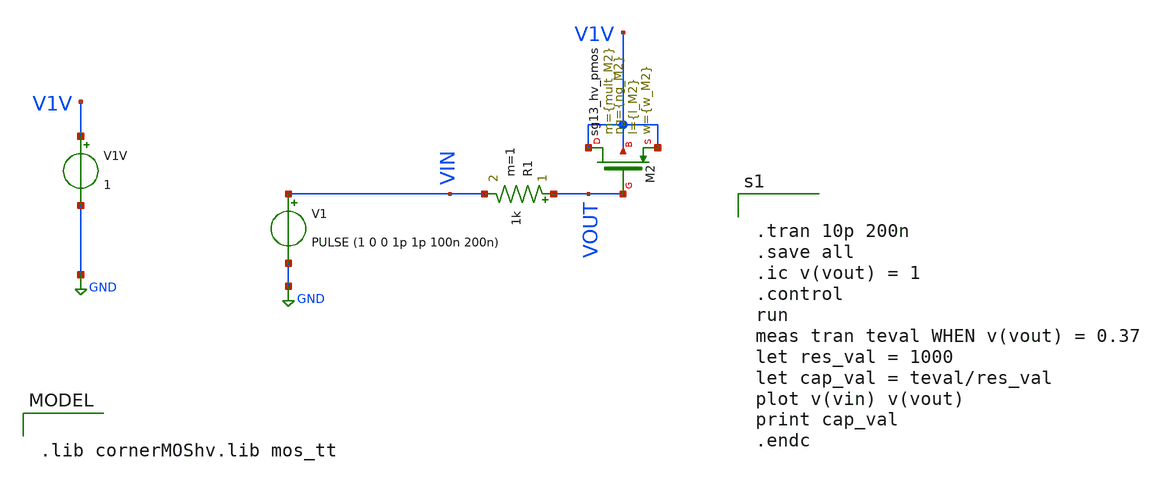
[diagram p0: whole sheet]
** sch_path: xschem/TB_hvPMOS_cgate-ext.sch
**.subckt TB_hvPMOS_cgate-ext
R1 VOUT VIN 1k m=1
V1 VIN GND PULSE (1 0 0 1p 1p 100n 200n)
XM2 V1V VOUT V1V V1V sg13_hv_pmos w={w_M2} l={l_M2} ng={ng_M2} m={mult_M2} mm_ok=1
V1V V1V GND 1
**** begin user architecture code


.tran 10p 200n
.save all
.ic v(vout) = 1
.control
run
meas tran teval WHEN v(vout) = 0.37
let res_val = 1000
let cap_val = teval/res_val
plot v(vin) v(vout)
print cap_val
.endc




.param temp=27

.param mult_M2 = 1200
.param w_M2 =10u
*.param l_M2 =0.25u
.param l_M2 =0.25u
.param ng_M2 =1






.lib cornerMOShv.lib mos_tt

**** end user architecture code
**.ends
.GLOBAL GND
.end
